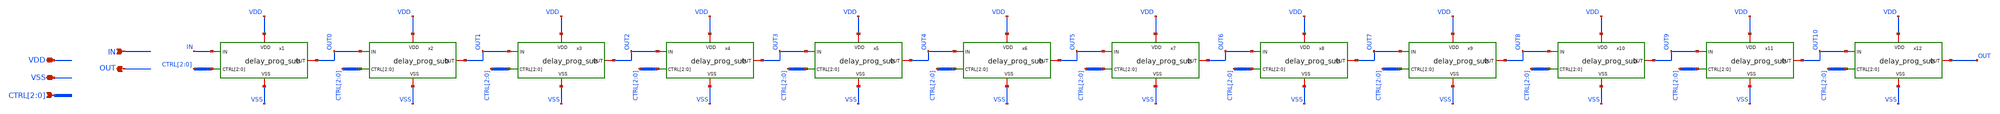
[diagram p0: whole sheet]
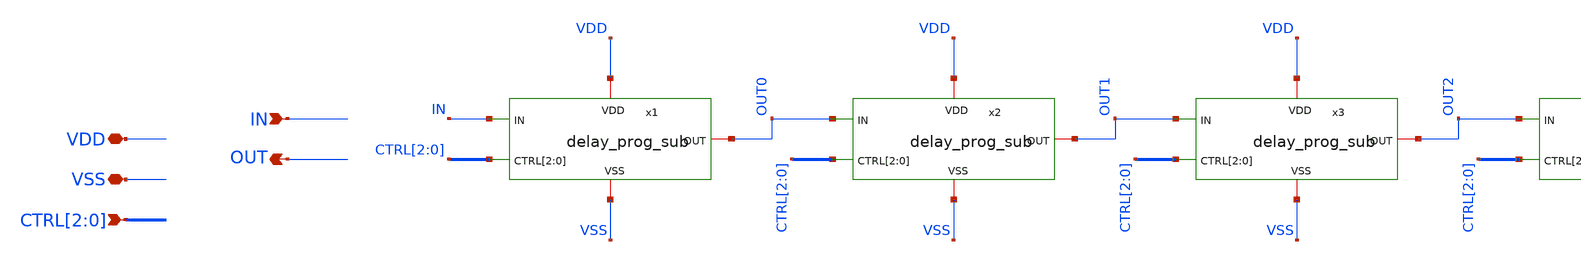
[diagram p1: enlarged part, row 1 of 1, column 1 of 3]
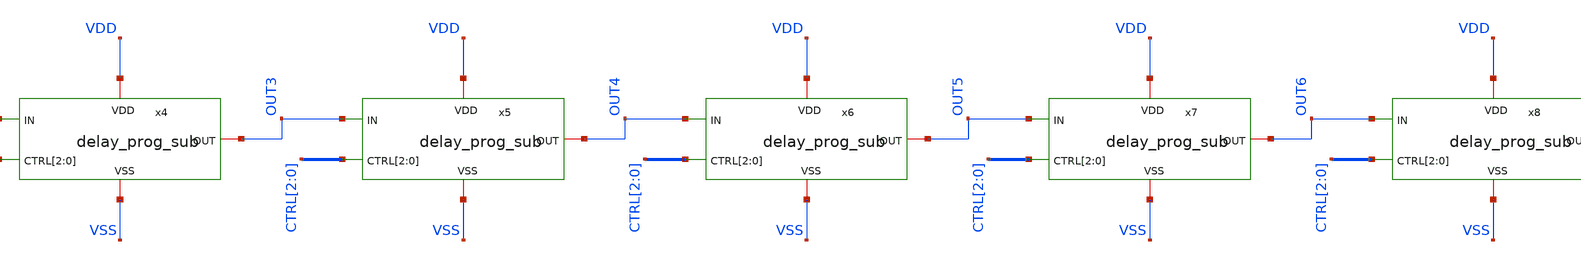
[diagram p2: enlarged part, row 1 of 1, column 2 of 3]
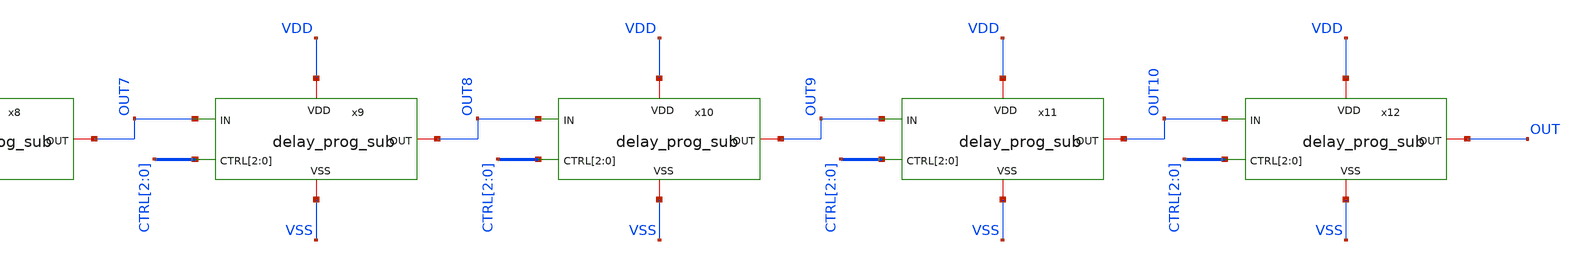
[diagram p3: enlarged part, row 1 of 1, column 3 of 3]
** sch_path: ADC8711-main/schematic/xschem/delay_prog.sch
**.subckt delay_prog IN VDD VSS CTRL[2],CTRL[1],CTRL[0] OUT
*.ipin IN
*.iopin VDD
*.iopin VSS
*.ipin CTRL[2],CTRL[1],CTRL[0]
*.opin OUT
x1 OUT0 IN VDD VSS CTRL[2] CTRL[1] CTRL[0] delay_prog_sub
x2 OUT1 OUT0 VDD VSS CTRL[2] CTRL[1] CTRL[0] delay_prog_sub
x3 OUT2 OUT1 VDD VSS CTRL[2] CTRL[1] CTRL[0] delay_prog_sub
x4 OUT3 OUT2 VDD VSS CTRL[2] CTRL[1] CTRL[0] delay_prog_sub
x5 OUT4 OUT3 VDD VSS CTRL[2] CTRL[1] CTRL[0] delay_prog_sub
x6 OUT5 OUT4 VDD VSS CTRL[2] CTRL[1] CTRL[0] delay_prog_sub
x7 OUT6 OUT5 VDD VSS CTRL[2] CTRL[1] CTRL[0] delay_prog_sub
x8 OUT7 OUT6 VDD VSS CTRL[2] CTRL[1] CTRL[0] delay_prog_sub
x9 OUT8 OUT7 VDD VSS CTRL[2] CTRL[1] CTRL[0] delay_prog_sub
x10 OUT9 OUT8 VDD VSS CTRL[2] CTRL[1] CTRL[0] delay_prog_sub
x11 OUT10 OUT9 VDD VSS CTRL[2] CTRL[1] CTRL[0] delay_prog_sub
x12 OUT OUT10 VDD VSS CTRL[2] CTRL[1] CTRL[0] delay_prog_sub
**.ends
.end
